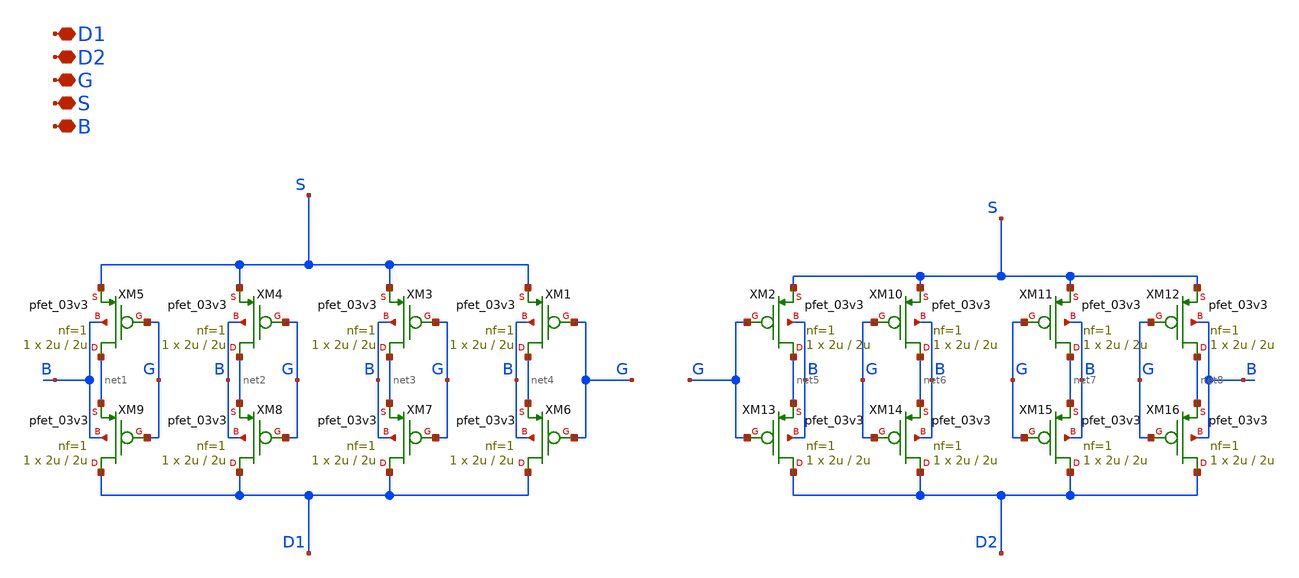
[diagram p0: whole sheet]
** sch_path: TIA/xschem/PseudoResistor/DiffN_pfets.sch
**.subckt DiffN_pfets D1 D2 G S B
*.iopin D1
*.iopin D2
*.iopin G
*.iopin S
*.iopin B
XM1 net4 G S B pfet_03v3 L=2u W=2u nf=1 ad='int((nf+1)/2) * W/nf * 0.18u' as='int((nf+2)/2) * W/nf * 0.18u'
+ pd='2*int((nf+1)/2) * (W/nf + 0.18u)' ps='2*int((nf+2)/2) * (W/nf + 0.18u)' nrd='0.18u / W' nrs='0.18u / W'
+ sa=0 sb=0 sd=0 m=1
XM2 net5 G S B pfet_03v3 L=2u W=2u nf=1 ad='int((nf+1)/2) * W/nf * 0.18u' as='int((nf+2)/2) * W/nf * 0.18u'
+ pd='2*int((nf+1)/2) * (W/nf + 0.18u)' ps='2*int((nf+2)/2) * (W/nf + 0.18u)' nrd='0.18u / W' nrs='0.18u / W'
+ sa=0 sb=0 sd=0 m=1
XM3 net3 G S B pfet_03v3 L=2u W=2u nf=1 ad='int((nf+1)/2) * W/nf * 0.18u' as='int((nf+2)/2) * W/nf * 0.18u'
+ pd='2*int((nf+1)/2) * (W/nf + 0.18u)' ps='2*int((nf+2)/2) * (W/nf + 0.18u)' nrd='0.18u / W' nrs='0.18u / W'
+ sa=0 sb=0 sd=0 m=1
XM4 net2 G S B pfet_03v3 L=2u W=2u nf=1 ad='int((nf+1)/2) * W/nf * 0.18u' as='int((nf+2)/2) * W/nf * 0.18u'
+ pd='2*int((nf+1)/2) * (W/nf + 0.18u)' ps='2*int((nf+2)/2) * (W/nf + 0.18u)' nrd='0.18u / W' nrs='0.18u / W'
+ sa=0 sb=0 sd=0 m=1
XM5 net1 G S B pfet_03v3 L=2u W=2u nf=1 ad='int((nf+1)/2) * W/nf * 0.18u' as='int((nf+2)/2) * W/nf * 0.18u'
+ pd='2*int((nf+1)/2) * (W/nf + 0.18u)' ps='2*int((nf+2)/2) * (W/nf + 0.18u)' nrd='0.18u / W' nrs='0.18u / W'
+ sa=0 sb=0 sd=0 m=1
XM6 D1 G net4 B pfet_03v3 L=2u W=2u nf=1 ad='int((nf+1)/2) * W/nf * 0.18u' as='int((nf+2)/2) * W/nf * 0.18u'
+ pd='2*int((nf+1)/2) * (W/nf + 0.18u)' ps='2*int((nf+2)/2) * (W/nf + 0.18u)' nrd='0.18u / W' nrs='0.18u / W'
+ sa=0 sb=0 sd=0 m=1
XM7 D1 G net3 B pfet_03v3 L=2u W=2u nf=1 ad='int((nf+1)/2) * W/nf * 0.18u' as='int((nf+2)/2) * W/nf * 0.18u'
+ pd='2*int((nf+1)/2) * (W/nf + 0.18u)' ps='2*int((nf+2)/2) * (W/nf + 0.18u)' nrd='0.18u / W' nrs='0.18u / W'
+ sa=0 sb=0 sd=0 m=1
XM8 D1 G net2 B pfet_03v3 L=2u W=2u nf=1 ad='int((nf+1)/2) * W/nf * 0.18u' as='int((nf+2)/2) * W/nf * 0.18u'
+ pd='2*int((nf+1)/2) * (W/nf + 0.18u)' ps='2*int((nf+2)/2) * (W/nf + 0.18u)' nrd='0.18u / W' nrs='0.18u / W'
+ sa=0 sb=0 sd=0 m=1
XM9 D1 G net1 B pfet_03v3 L=2u W=2u nf=1 ad='int((nf+1)/2) * W/nf * 0.18u' as='int((nf+2)/2) * W/nf * 0.18u'
+ pd='2*int((nf+1)/2) * (W/nf + 0.18u)' ps='2*int((nf+2)/2) * (W/nf + 0.18u)' nrd='0.18u / W' nrs='0.18u / W'
+ sa=0 sb=0 sd=0 m=1
XM10 net6 G S B pfet_03v3 L=2u W=2u nf=1 ad='int((nf+1)/2) * W/nf * 0.18u' as='int((nf+2)/2) * W/nf * 0.18u'
+ pd='2*int((nf+1)/2) * (W/nf + 0.18u)' ps='2*int((nf+2)/2) * (W/nf + 0.18u)' nrd='0.18u / W' nrs='0.18u / W'
+ sa=0 sb=0 sd=0 m=1
XM11 net7 G S B pfet_03v3 L=2u W=2u nf=1 ad='int((nf+1)/2) * W/nf * 0.18u' as='int((nf+2)/2) * W/nf * 0.18u'
+ pd='2*int((nf+1)/2) * (W/nf + 0.18u)' ps='2*int((nf+2)/2) * (W/nf + 0.18u)' nrd='0.18u / W' nrs='0.18u / W'
+ sa=0 sb=0 sd=0 m=1
XM12 net8 G S B pfet_03v3 L=2u W=2u nf=1 ad='int((nf+1)/2) * W/nf * 0.18u' as='int((nf+2)/2) * W/nf * 0.18u'
+ pd='2*int((nf+1)/2) * (W/nf + 0.18u)' ps='2*int((nf+2)/2) * (W/nf + 0.18u)' nrd='0.18u / W' nrs='0.18u / W'
+ sa=0 sb=0 sd=0 m=1
XM13 D2 G net5 B pfet_03v3 L=2u W=2u nf=1 ad='int((nf+1)/2) * W/nf * 0.18u' as='int((nf+2)/2) * W/nf * 0.18u'
+ pd='2*int((nf+1)/2) * (W/nf + 0.18u)' ps='2*int((nf+2)/2) * (W/nf + 0.18u)' nrd='0.18u / W' nrs='0.18u / W'
+ sa=0 sb=0 sd=0 m=1
XM14 D2 G net6 B pfet_03v3 L=2u W=2u nf=1 ad='int((nf+1)/2) * W/nf * 0.18u' as='int((nf+2)/2) * W/nf * 0.18u'
+ pd='2*int((nf+1)/2) * (W/nf + 0.18u)' ps='2*int((nf+2)/2) * (W/nf + 0.18u)' nrd='0.18u / W' nrs='0.18u / W'
+ sa=0 sb=0 sd=0 m=1
XM15 D2 G net7 B pfet_03v3 L=2u W=2u nf=1 ad='int((nf+1)/2) * W/nf * 0.18u' as='int((nf+2)/2) * W/nf * 0.18u'
+ pd='2*int((nf+1)/2) * (W/nf + 0.18u)' ps='2*int((nf+2)/2) * (W/nf + 0.18u)' nrd='0.18u / W' nrs='0.18u / W'
+ sa=0 sb=0 sd=0 m=1
XM16 D2 G net8 B pfet_03v3 L=2u W=2u nf=1 ad='int((nf+1)/2) * W/nf * 0.18u' as='int((nf+2)/2) * W/nf * 0.18u'
+ pd='2*int((nf+1)/2) * (W/nf + 0.18u)' ps='2*int((nf+2)/2) * (W/nf + 0.18u)' nrd='0.18u / W' nrs='0.18u / W'
+ sa=0 sb=0 sd=0 m=1
**.ends
.end
